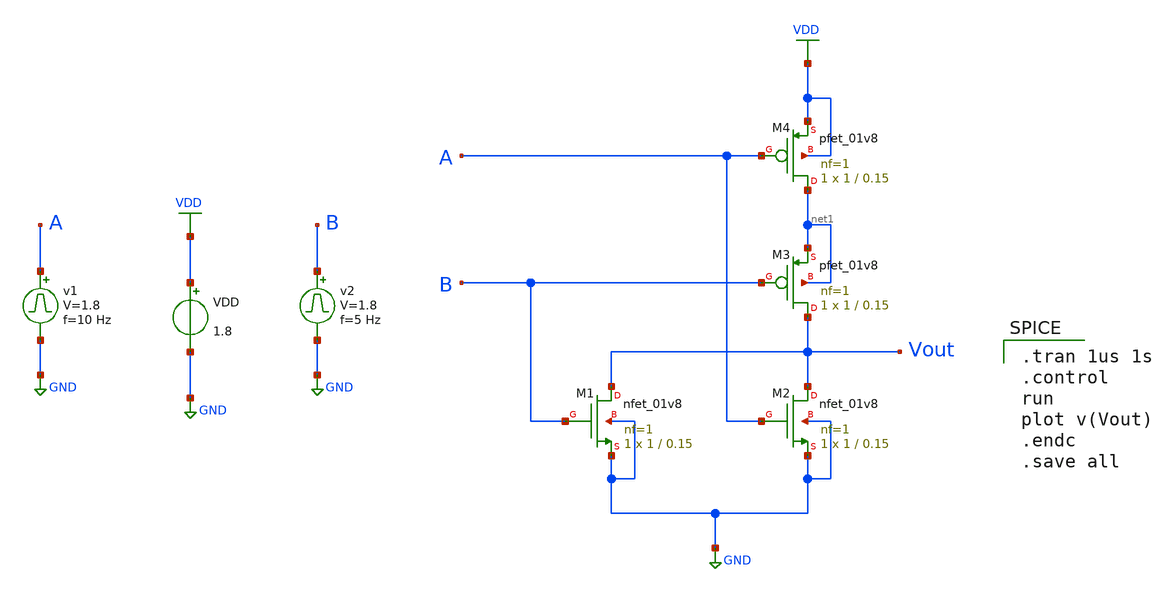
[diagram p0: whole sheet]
** sch_path: Circuits/Examples/Digital/NOR/NOR_gate.sch
**.subckt NOR_gate
XM1 Vout B GND GND sky130_fd_pr__nfet_01v8 L=0.15 W=1 nf=1 ad='int((nf+1)/2) * W/nf * 0.29' as='int((nf+2)/2) * W/nf * 0.29'
+ pd='2*int((nf+1)/2) * (W/nf + 0.29)' ps='2*int((nf+2)/2) * (W/nf + 0.29)' nrd='0.29 / W' nrs='0.29 / W'
+ sa=0 sb=0 sd=0 mult=1 m=1
XM2 Vout A GND GND sky130_fd_pr__nfet_01v8 L=0.15 W=1 nf=1 ad='int((nf+1)/2) * W/nf * 0.29' as='int((nf+2)/2) * W/nf * 0.29'
+ pd='2*int((nf+1)/2) * (W/nf + 0.29)' ps='2*int((nf+2)/2) * (W/nf + 0.29)' nrd='0.29 / W' nrs='0.29 / W'
+ sa=0 sb=0 sd=0 mult=1 m=1
XM3 Vout B net1 net1 sky130_fd_pr__pfet_01v8 L=0.15 W=1 nf=1 ad='int((nf+1)/2) * W/nf * 0.29' as='int((nf+2)/2) * W/nf * 0.29'
+ pd='2*int((nf+1)/2) * (W/nf + 0.29)' ps='2*int((nf+2)/2) * (W/nf + 0.29)' nrd='0.29 / W' nrs='0.29 / W'
+ sa=0 sb=0 sd=0 mult=1 m=1
XM4 net1 A VDD VDD sky130_fd_pr__pfet_01v8 L=0.15 W=1 nf=1 ad='int((nf+1)/2) * W/nf * 0.29' as='int((nf+2)/2) * W/nf * 0.29'
+ pd='2*int((nf+1)/2) * (W/nf + 0.29)' ps='2*int((nf+2)/2) * (W/nf + 0.29)' nrd='0.29 / W' nrs='0.29 / W'
+ sa=0 sb=0 sd=0 mult=1 m=1
VDD VDD GND 1.8
v1 A GND pulse 0 1.8 '0.495/ 10 ' '0.01/10 ' '0.01/10 ' '0.49/10 ' '1/10 '
v2 B GND pulse 0 1.8 '0.495/ 5 ' '0.01/5 ' '0.01/5 ' '0.49/5 ' '1/5 '
**** begin user architecture code
 ** manual skywater pdks install (with patches applied)
* .lib $::SKYWATER_MODELS/models/sky130.lib.spice tt

** opencircuitdesign pdks install
.lib $::SKYWATER_MODELS/sky130.lib.spice tt

.param mc_mm_switch=0
.param mc_pr_switch=0


.tran 1us 1s
.control
run
plot v(Vout)
.endc
.save all

**** end user architecture code
**.ends
.GLOBAL GND
.GLOBAL VDD
.end
